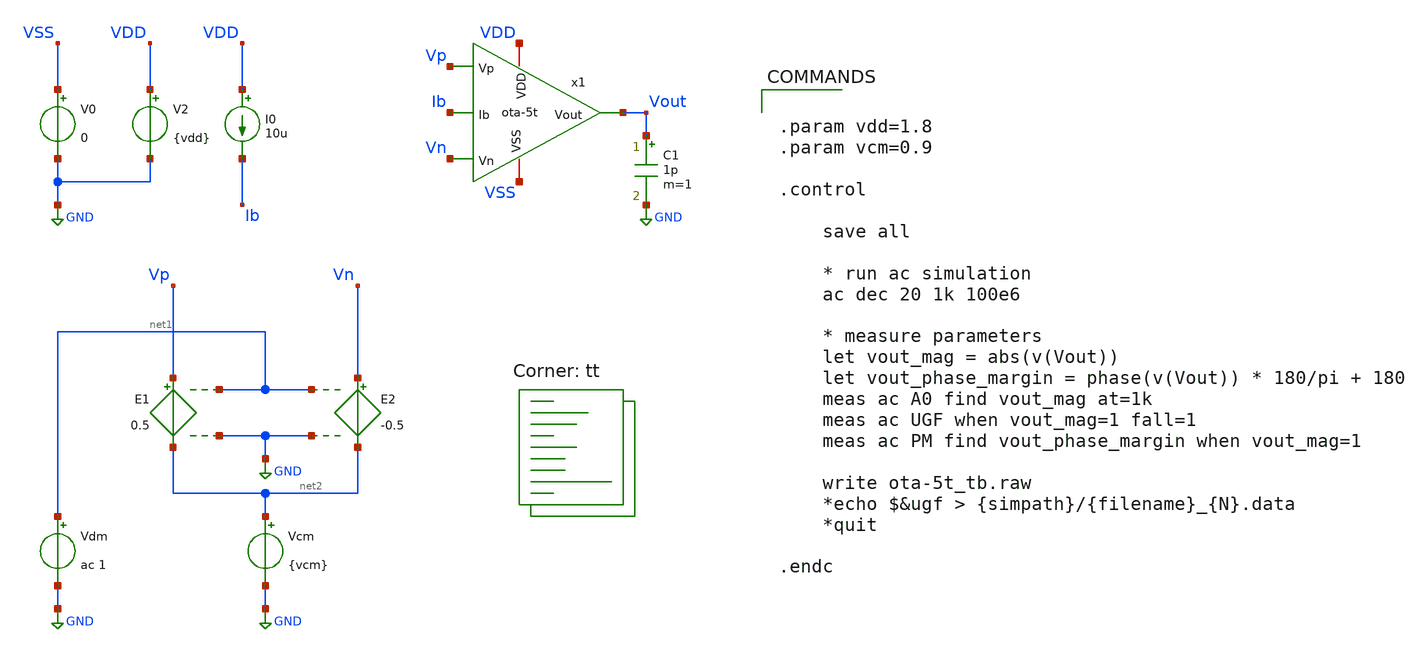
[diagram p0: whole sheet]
** sch_path: xschem/ota-5t_tb.sch
**.subckt ota-5t_tb
I0 VDD Ib 10u
C1 Vout GND 1p m=1
x1 Vp Vn Vout VDD VSS Ib ota-5t
V0 VSS GND 0
V2 VDD GND {vdd}
E1 Vp net2 net1 GND 0.5
E2 Vn net2 net1 GND -0.5
Vdm net1 GND ac 1
Vcm net2 GND {vcm}
**** begin user architecture code


.param vdd=1.8
.param vcm=0.9

.control

    save all

    * run ac simulation
    ac dec 20 1k 100e6

    * measure parameters
    let vout_mag = abs(v(Vout))
    let vout_phase_margin = phase(v(Vout)) * 180/pi + 180
    meas ac A0 find vout_mag at=1k
    meas ac UGF when vout_mag=1 fall=1
    meas ac PM find vout_phase_margin when vout_mag=1

    write ota-5t_tb.raw
    *echo $&ugf > {simpath}/{filename}_{N}.data
    *quit

.endc


.lib $::SKYWATER_MODELS/sky130.lib.spice tt
**** end user architecture code
**.ends
.GLOBAL GND
.end
